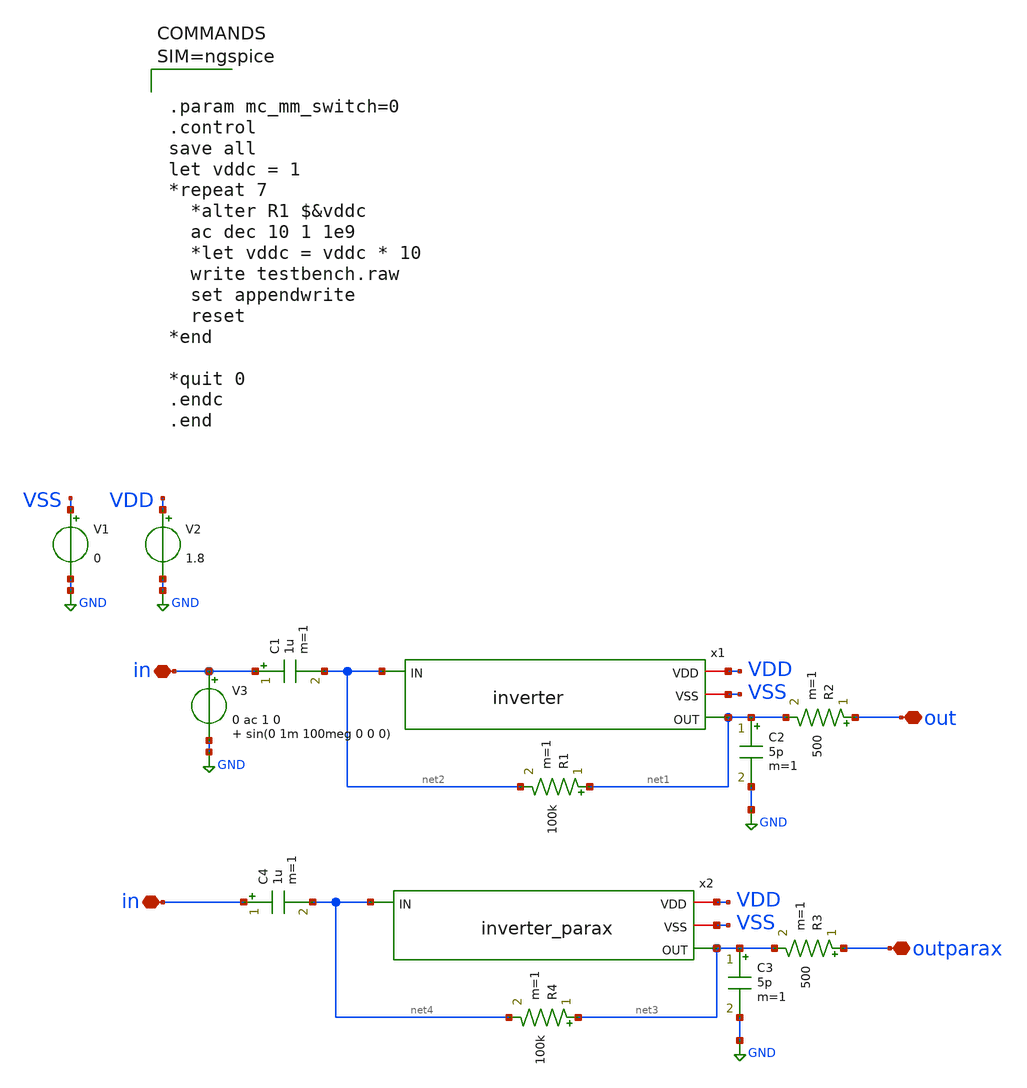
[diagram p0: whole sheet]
** sch_path: xschem/testbench.sch
**.subckt testbench in out in outparax
*.iopin in
*.iopin out
*.iopin in
*.iopin outparax
V1 VSS GND 0
V2 VDD GND 1.8
R2 out net1 500 m=1
C2 net1 GND 5p m=1
V3 in GND 0 ac 1 0 sin(0 1m 100meg 0 0 0)
x1 VDD VSS net1 net2 inverter
C1 in net2 1u m=1
R1 net1 net2 100k m=1
R3 outparax net3 500 m=1
C3 net3 GND 5p m=1
x2 VDD VSS net3 net4 inverter_parax
C4 in net4 1u m=1
R4 net3 net4 100k m=1
**** begin user architecture code

** opencircuitdesign pdks install
.lib $::SKYWATER_MODELS/sky130.lib.spice tt




.param mc_mm_switch=0
.control
save all
let vddc = 1
*repeat 7
  *alter R1 $&vddc
  ac dec 10 1 1e9
  *let vddc = vddc * 10
  write testbench.raw
  set appendwrite
  reset
*end

*quit 0
.endc
.end



**** end user architecture code
**.ends

* expanding   symbol:  inverter.sym # of pins=4
** sym_path: xschem/inverter.sym
** sch_path: xschem/inverter.sch
.subckt inverter VDD VSS OUT IN
*.iopin VDD
*.iopin VSS
*.ipin IN
*.opin OUT
XM1 OUT IN VDD VDD sky130_fd_pr__pfet_01v8 L=1 W=10 nf=1 ad='int((nf+1)/2) * W/nf * 0.29' as='int((nf+2)/2) * W/nf * 0.29'
+ pd='2*int((nf+1)/2) * (W/nf + 0.29)' ps='2*int((nf+2)/2) * (W/nf + 0.29)' nrd='0.29 / W' nrs='0.29 / W'
+ sa=0 sb=0 sd=0 mult=1 m=1
XM2 OUT IN VSS VSS sky130_fd_pr__nfet_01v8 L=1 W=10 nf=1 ad='int((nf+1)/2) * W/nf * 0.29' as='int((nf+2)/2) * W/nf * 0.29'
+ pd='2*int((nf+1)/2) * (W/nf + 0.29)' ps='2*int((nf+2)/2) * (W/nf + 0.29)' nrd='0.29 / W' nrs='0.29 / W'
+ sa=0 sb=0 sd=0 mult=1 m=1
.ends


* expanding   symbol:  inverter_parax.sym # of pins=4
** sym_path: xschem/inverter.sym
.include [file normalize ../mag/inverter.sim.spice]
.GLOBAL GND
.end
